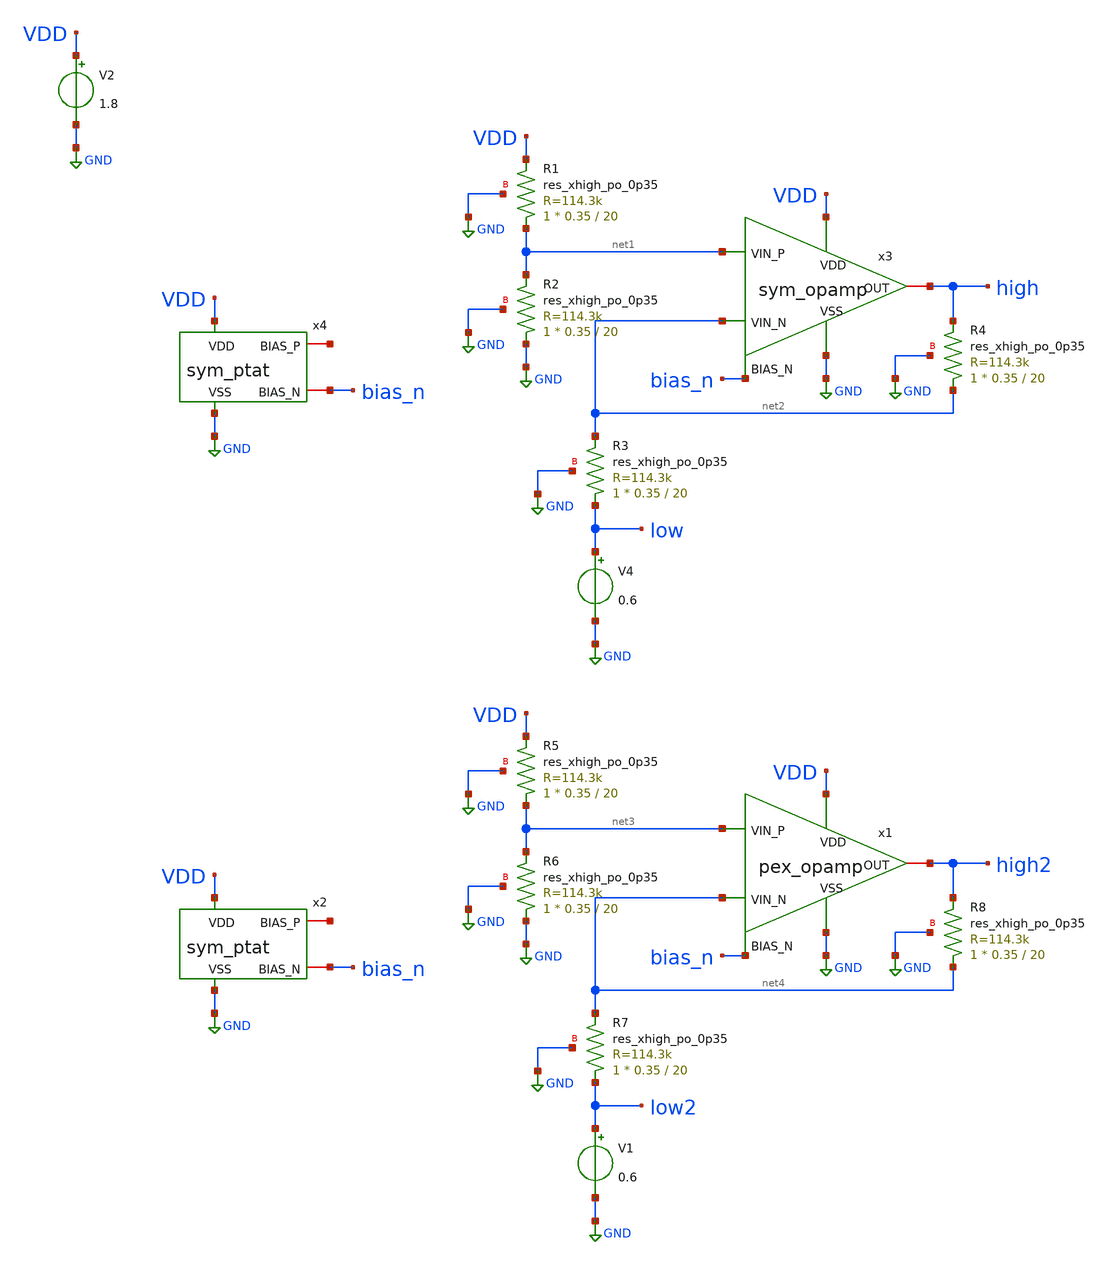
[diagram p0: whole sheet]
** sch_path: schem/tb/tb_opamp.sch
**.subckt tb_opamp
V2 VDD GND 1.8
x3 VDD GND net1 net2 high bias_n sym_opamp
V4 low GND 0.6
x4 VDD GND net5 bias_n sym_ptat
XR1 net1 VDD GND sky130_fd_pr__res_xhigh_po_0p35 L=20 mult=1 m=1
XR2 GND net1 GND sky130_fd_pr__res_xhigh_po_0p35 L=20 mult=1 m=1
XR3 low net2 GND sky130_fd_pr__res_xhigh_po_0p35 L=20 mult=1 m=1
XR4 net2 high GND sky130_fd_pr__res_xhigh_po_0p35 L=20 mult=1 m=1
V1 low2 GND 0.6
x2 VDD GND net6 bias_n sym_ptat
XR5 net3 VDD GND sky130_fd_pr__res_xhigh_po_0p35 L=20 mult=1 m=1
XR6 GND net3 GND sky130_fd_pr__res_xhigh_po_0p35 L=20 mult=1 m=1
XR7 low2 net4 GND sky130_fd_pr__res_xhigh_po_0p35 L=20 mult=1 m=1
XR8 net4 high2 GND sky130_fd_pr__res_xhigh_po_0p35 L=20 mult=1 m=1
x1 VDD GND net3 net4 high2 bias_n opamp
**** begin user architecture code


.include /home/zhixuan/projects/fyp_vco/magic/ip/opamp/opamp.spice
.lib /usr/local/share/pdk/sky130A/libs.tech/ngspice/sky130.lib.spice tt

.tran 1u 5m
.save all
.op

.control
    run
    plot 1.8 0 0.9 high low high2 low2
.endc

.end


**** end user architecture code
**.ends

* expanding   symbol:  sym_opamp.sym # of pins=6
** sym_path: schem/symbol_repo/sym_opamp.sym
** sch_path: schem/symbol_repo/sym_opamp.sch
.subckt sym_opamp VDD VSS VIN_P VIN_N OUT BIAS_N
*.ipin VDD
*.ipin VSS
*.ipin BIAS_N
*.iopin OUT
*.ipin VIN_N
*.ipin VIN_P
XMN_vinn net1 VIN_N net3 VSS sky130_fd_pr__nfet_01v8 L=0.5 W=1 nf=1 ad='int((1 + 1)/2) * 1 / 1 * 0.29'
+ as='int((1 + 2)/2) * 1 / 1 * 0.29' pd='2*int((1 + 1)/2) * (1 / 1 + 0.29)' ps='2*int((1 + 2)/2) * (1 / 1 + 0.29)'
+ nrd='0.29 / 1 ' nrs='0.29 / 1 ' sa=0 sb=0 sd=0 mult=1 m=1
XMP_cs_1 net2 net1 VDD VDD sky130_fd_pr__pfet_01v8 L=0.5 W=2 nf=1 ad='int((1 + 1)/2) * 2 / 1 * 0.29'
+ as='int((1 + 2)/2) * 2 / 1 * 0.29' pd='2*int((1 + 1)/2) * (2 / 1 + 0.29)' ps='2*int((1 + 2)/2) * (2 / 1 + 0.29)'
+ nrd='0.29 / 2 ' nrs='0.29 / 2 ' sa=0 sb=0 sd=0 mult=1 m=1
XMP_diode net1 net1 VDD VDD sky130_fd_pr__pfet_01v8 L=0.5 W=2 nf=1 ad='int((1 + 1)/2) * 2 / 1 * 0.29'
+ as='int((1 + 2)/2) * 2 / 1 * 0.29' pd='2*int((1 + 1)/2) * (2 / 1 + 0.29)' ps='2*int((1 + 2)/2) * (2 / 1 + 0.29)'
+ nrd='0.29 / 2 ' nrs='0.29 / 2 ' sa=0 sb=0 sd=0 mult=1 m=1
XMN_vinp net2 VIN_P net3 VSS sky130_fd_pr__nfet_01v8 L=0.5 W=1 nf=1 ad='int((1 + 1)/2) * 1 / 1 * 0.29'
+ as='int((1 + 2)/2) * 1 / 1 * 0.29' pd='2*int((1 + 1)/2) * (1 / 1 + 0.29)' ps='2*int((1 + 2)/2) * (1 / 1 + 0.29)'
+ nrd='0.29 / 1 ' nrs='0.29 / 1 ' sa=0 sb=0 sd=0 mult=1 m=1
XMN_tail_1 net3 BIAS_N VSS GND sky130_fd_pr__nfet_01v8 L=0.75 W=2 nf=1 ad='int((1 + 1)/2) * 2 / 1 * 0.29'
+ as='int((1 + 2)/2) * 2 / 1 * 0.29' pd='2*int((1 + 1)/2) * (2 / 1 + 0.29)' ps='2*int((1 + 2)/2) * (2 / 1 + 0.29)'
+ nrd='0.29 / 2 ' nrs='0.29 / 2 ' sa=0 sb=0 sd=0 mult=1 m=1
XMP_cs_2 OUT net2 VDD VDD sky130_fd_pr__pfet_01v8 L=0.5 W=2 nf=1 ad='int((1 + 1)/2) * 2 / 1 * 0.29' as='int((1 + 2)/2) * 2 / 1 * 0.29'
+ pd='2*int((1 + 1)/2) * (2 / 1 + 0.29)' ps='2*int((1 + 2)/2) * (2 / 1 + 0.29)' nrd='0.29 / 2 ' nrs='0.29 / 2 '
+ sa=0 sb=0 sd=0 mult=1 m=1
XMN_tail_2 OUT BIAS_N VSS VSS sky130_fd_pr__nfet_01v8 L=0.75 W=2 nf=1 ad='int((1 + 1)/2) * 2 / 1 * 0.29'
+ as='int((1 + 2)/2) * 2 / 1 * 0.29' pd='2*int((1 + 1)/2) * (2 / 1 + 0.29)' ps='2*int((1 + 2)/2) * (2 / 1 + 0.29)'
+ nrd='0.29 / 2 ' nrs='0.29 / 2 ' sa=0 sb=0 sd=0 mult=1 m=1
XCc net4 OUT sky130_fd_pr__cap_mim_m3_1 W=4 L=4 MF=1 m=1
XR1 net4 net2 VSS sky130_fd_pr__res_xhigh_po_0p35 L=2 mult=1 m=1
.ends


* expanding   symbol:  sym_ptat.sym # of pins=4
** sym_path: schem/symbol_repo/sym_ptat.sym
** sch_path: schem/symbol_repo/sym_ptat.sch
.subckt sym_ptat VDD VSS BIAS_P BIAS_N
*.ipin VDD
*.ipin VSS
*.iopin BIAS_P
*.iopin BIAS_N
XMN_ptat2 net6 net1 net2 VSS sky130_fd_pr__nfet_01v8 L=0.5 W=2 nf=2 ad='int((2 + 1)/2) * 2 / 2 * 0.29'
+ as='int((2 + 2)/2) * 2 / 2 * 0.29' pd='2*int((2 + 1)/2) * (2 / 2 + 0.29)' ps='2*int((2 + 2)/2) * (2 / 2 + 0.29)'
+ nrd='0.29 / 2 ' nrs='0.29 / 2 ' sa=0 sb=0 sd=0 mult=1 m=1
XMP_diode1 net3 BIAS_P VDD VDD sky130_fd_pr__pfet_01v8 L=0.5 W=2 nf=2 ad='int((2 + 1)/2) * 2 / 2 * 0.29'
+ as='int((2 + 2)/2) * 2 / 2 * 0.29' pd='2*int((2 + 1)/2) * (2 / 2 + 0.29)' ps='2*int((2 + 2)/2) * (2 / 2 + 0.29)'
+ nrd='0.29 / 2 ' nrs='0.29 / 2 ' sa=0 sb=0 sd=0 mult=1 m=1
XMP_mir1_l net4 BIAS_P VDD VDD sky130_fd_pr__pfet_01v8 L=0.5 W=2 nf=2 ad='int((2 + 1)/2) * 2 / 2 * 0.29'
+ as='int((2 + 2)/2) * 2 / 2 * 0.29' pd='2*int((2 + 1)/2) * (2 / 2 + 0.29)' ps='2*int((2 + 2)/2) * (2 / 2 + 0.29)'
+ nrd='0.29 / 2 ' nrs='0.29 / 2 ' sa=0 sb=0 sd=0 mult=1 m=1
XMN_diode2 net5 net1 VSS VSS sky130_fd_pr__nfet_01v8 L=0.5 W=2 nf=4 ad='int((4 + 1)/2) * 2 / 4 * 0.29'
+ as='int((4 + 2)/2) * 2 / 4 * 0.29' pd='2*int((4 + 1)/2) * (2 / 4 + 0.29)' ps='2*int((4 + 2)/2) * (2 / 4 + 0.29)'
+ nrd='0.29 / 2 ' nrs='0.29 / 2 ' sa=0 sb=0 sd=0 mult=1 m=1
XMP_inv BIAS_N BIAS_P VDD VDD sky130_fd_pr__pfet_01v8 L=0.75 W=2 nf=5 ad='int((5 + 1)/2) * 2 / 5 * 0.29'
+ as='int((5 + 2)/2) * 2 / 5 * 0.29' pd='2*int((5 + 1)/2) * (2 / 5 + 0.29)' ps='2*int((5 + 2)/2) * (2 / 5 + 0.29)'
+ nrd='0.29 / 2 ' nrs='0.29 / 2 ' sa=0 sb=0 sd=0 mult=1 m=1
XMP_diode2 BIAS_P BIAS_P net3 VDD sky130_fd_pr__pfet_01v8 L=0.5 W=2 nf=2 ad='int((2 + 1)/2) * 2 / 2 * 0.29'
+ as='int((2 + 2)/2) * 2 / 2 * 0.29' pd='2*int((2 + 1)/2) * (2 / 2 + 0.29)' ps='2*int((2 + 2)/2) * (2 / 2 + 0.29)'
+ nrd='0.29 / 2 ' nrs='0.29 / 2 ' sa=0 sb=0 sd=0 mult=1 m=1
XMP_mir2_l net1 BIAS_P net4 VDD sky130_fd_pr__pfet_01v8 L=0.5 W=2 nf=2 ad='int((2 + 1)/2) * 2 / 2 * 0.29'
+ as='int((2 + 2)/2) * 2 / 2 * 0.29' pd='2*int((2 + 1)/2) * (2 / 2 + 0.29)' ps='2*int((2 + 2)/2) * (2 / 2 + 0.29)'
+ nrd='0.29 / 2 ' nrs='0.29 / 2 ' sa=0 sb=0 sd=0 mult=1 m=1
XMN_ptat1 BIAS_P net1 net6 VSS sky130_fd_pr__nfet_01v8 L=0.5 W=2 nf=2 ad='int((2 + 1)/2) * 2 / 2 * 0.29'
+ as='int((2 + 2)/2) * 2 / 2 * 0.29' pd='2*int((2 + 1)/2) * (2 / 2 + 0.29)' ps='2*int((2 + 2)/2) * (2 / 2 + 0.29)'
+ nrd='0.29 / 2 ' nrs='0.29 / 2 ' sa=0 sb=0 sd=0 mult=1 m=1
XMN_diode1 net1 net1 net5 VSS sky130_fd_pr__nfet_01v8 L=0.5 W=2 nf=4 ad='int((4 + 1)/2) * 2 / 4 * 0.29'
+ as='int((4 + 2)/2) * 2 / 4 * 0.29' pd='2*int((4 + 1)/2) * (2 / 4 + 0.29)' ps='2*int((4 + 2)/2) * (2 / 4 + 0.29)'
+ nrd='0.29 / 2 ' nrs='0.29 / 2 ' sa=0 sb=0 sd=0 mult=1 m=1
XMN_inv BIAS_N BIAS_N VSS VSS sky130_fd_pr__nfet_01v8 L=0.75 W=2.5 nf=2 ad='int((2 + 1)/2) * 2.5 / 2 * 0.29'
+ as='int((2 + 2)/2) * 2.5 / 2 * 0.29' pd='2*int((2 + 1)/2) * (2.5 / 2 + 0.29)' ps='2*int((2 + 2)/2) * (2.5 / 2 + 0.29)'
+ nrd='0.29 / 2.5 ' nrs='0.29 / 2.5 ' sa=0 sb=0 sd=0 mult=1 m=1
XR1 VSS net2 VSS sky130_fd_pr__res_xhigh_po_0p35 L=2.8 mult=1 m=1
XMP_startup net1 VSS VDD VDD sky130_fd_pr__pfet_01v8 L=13 W=1 nf=1 ad='int((1 + 1)/2) * 1 / 1 * 0.29'
+ as='int((1 + 2)/2) * 1 / 1 * 0.29' pd='2*int((1 + 1)/2) * (1 / 1 + 0.29)' ps='2*int((1 + 2)/2) * (1 / 1 + 0.29)'
+ nrd='0.29 / 1 ' nrs='0.29 / 1 ' sa=0 sb=0 sd=0 mult=1 m=1
XMN_diode3 net7 net1 VSS VSS sky130_fd_pr__nfet_01v8 L=0.5 W=2 nf=4 ad='int((4 + 1)/2) * 2 / 4 * 0.29'
+ as='int((4 + 2)/2) * 2 / 4 * 0.29' pd='2*int((4 + 1)/2) * (2 / 4 + 0.29)' ps='2*int((4 + 2)/2) * (2 / 4 + 0.29)'
+ nrd='0.29 / 2 ' nrs='0.29 / 2 ' sa=0 sb=0 sd=0 mult=1 m=1
XMN_diode4 net1 net1 net7 VSS sky130_fd_pr__nfet_01v8 L=0.5 W=2 nf=4 ad='int((4 + 1)/2) * 2 / 4 * 0.29'
+ as='int((4 + 2)/2) * 2 / 4 * 0.29' pd='2*int((4 + 1)/2) * (2 / 4 + 0.29)' ps='2*int((4 + 2)/2) * (2 / 4 + 0.29)'
+ nrd='0.29 / 2 ' nrs='0.29 / 2 ' sa=0 sb=0 sd=0 mult=1 m=1
.ends

.GLOBAL GND
.end
